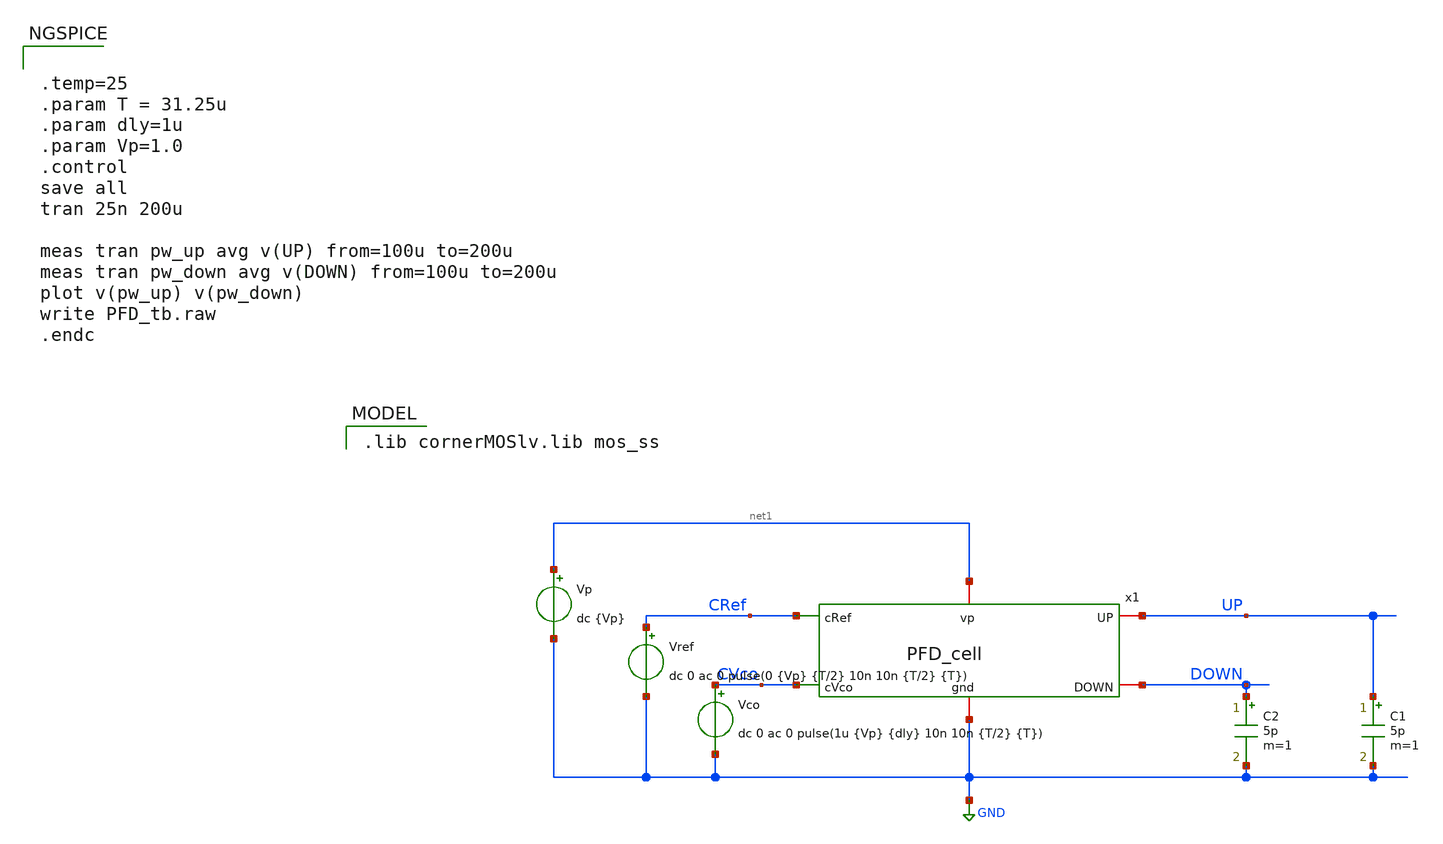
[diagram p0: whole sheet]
** sch_path: schematics/PFD/PFD_tb.sch
**.subckt PFD_tb
Vref CRef GND dc 0 ac 0 pulse(0 {Vp} {T/2} 10n 10n {T/2} {T})
Vco CVco GND dc 0 ac 0 pulse(1u {Vp} {dly} 10n 10n {T/2} {T})
Vp net1 GND dc {Vp}
C1 UP GND 5p m=1
C2 DOWN GND 5p m=1
x1 GND net1 CRef UP DOWN CVco PFD_cell
**** begin user architecture code
 .lib cornerMOSlv.lib mos_ss



.temp=25
.param T = 31.25u
.param dly=1u
.param Vp=1.0
.control
save all
tran 25n 200u

meas tran pw_up avg v(UP) from=100u to=200u
meas tran pw_down avg v(DOWN) from=100u to=200u
plot v(pw_up) v(pw_down)
write PFD_tb.raw
.endc


**** end user architecture code
**.ends
.GLOBAL GND
.end
